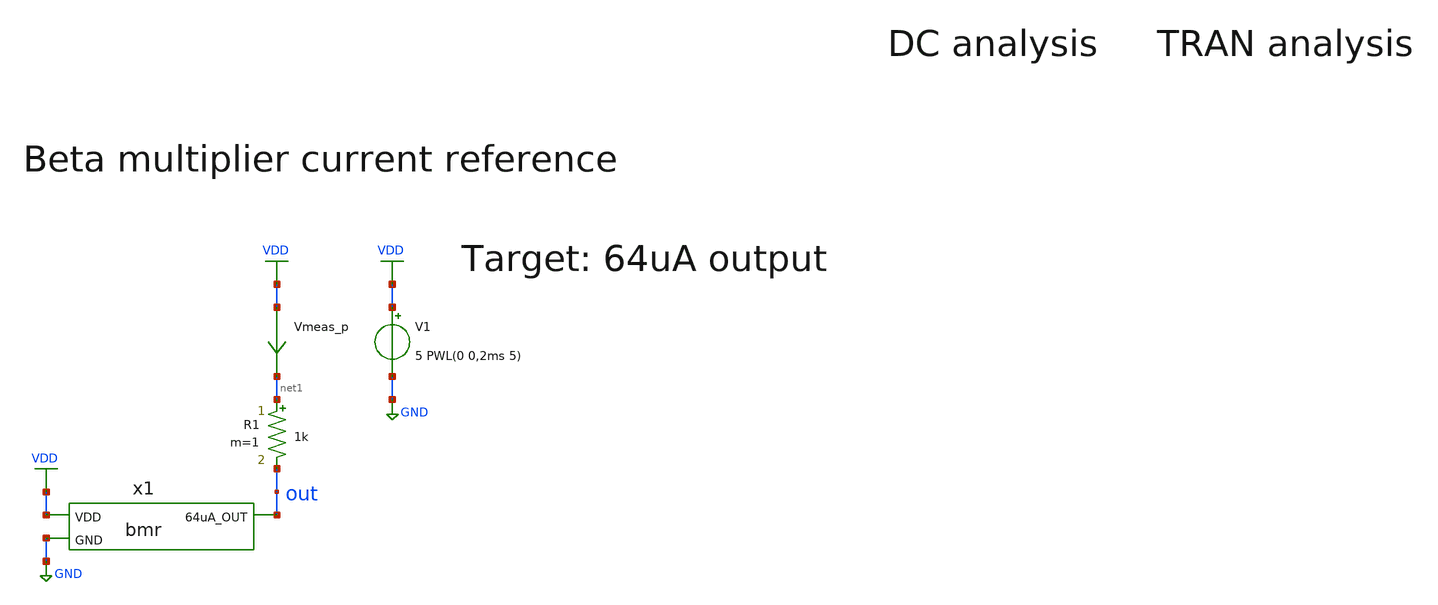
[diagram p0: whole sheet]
** sch_path: member_project/AM_Radio/Yamada3/xschem/tb_bmr.sch
* Copyright 2022 GlobalFoundries PDK Authors
* Licensed under the Apache License, Version 2.0 (the "License");
* you may not use this file except in compliance with the License.
* You may obtain a copy of the License at
* https://www.apache.org/licenses/LICENSE-2.0
* Unless required by applicable law or agreed to in writing, software
* distributed under the License is distributed on an "AS IS" BASIS,
* WITHOUT WARRANTIES OR CONDITIONS OF ANY KIND, either express or implied.
* See the License for the specific language governing permissions and
* limitations under the License.
**.subckt tb_bmr
V1 VDD GND 5 PWL(0 0,2ms 5)
Vmeas_p VDD net1 0
.save i(vmeas_p)
x1 VDD GND out bmr
R1 net1 out 1k m=1
**** begin user architecture code


.control
save all
save currents
* DC analysis
dc v1 0 5.5 0.1 r1 1k 50k 5k
write tb_bmr_dc.raw
meas dc current_p find i(vmeas_p) at=5

* TRANS analysis
tran 1u 5m
write tb_bmr_tran.raw
.endc


 .include $::LIB/ip62_models
**** end user architecture code
**.ends

* expanding   symbol:  bmr.sym # of pins=3
** sym_path: bmr.sym
** sch_path: bmr.sch
.subckt bmr VDD GND 64uA_OUT
*.ipin VDD
*.ipin GND
*.opin 64uA_OUT
XXM1 net3 net3 VDD VDD PMOS w=4u l=4u as=0 ad=0 ps=0 pd=0 nrd=0 nrs=0 m=1
XXM2 net3 net6 GND GND NMOS w=10u l=2u as=0 ad=0 ps=0 pd=0 nrd=0 nrs=0 m=1
XXM3 net4 net3 net6 GND NMOS w=10u l=1u as=0 ad=0 ps=0 pd=0 nrd=0 nrs=0 m=1
XXM4 net6 net4 net1 net1 PMOS w=30u l=2u as=0 ad=0 ps=0 pd=0 nrd=0 nrs=0 m=1
XXM5 net4 net4 net2 net2 PMOS w=30u l=2u as=0 ad=0 ps=0 pd=0 nrd=0 nrs=0 m=1
XXM7 net6 net6 GND GND NMOS w=10u l=2u as=0 ad=0 ps=0 pd=0 nrd=0 nrs=0 m=1
XXM8 net4 net6 net5 net5 NMOS w=40u l=2u as=0 ad=0 ps=0 pd=0 nrd=0 nrs=0 m=1
XR1 net5 GND VDD F_RR w=4e-06 R=1 l=27e-06 tc1=0 tc2=0
XXM6 net8 net4 net7 net7 PMOS w=30u l=2u as=0 ad=0 ps=0 pd=0 nrd=0 nrs=0 m=1
XXM9 net8 net8 net9 GND NMOS w=10u l=2u as=0 ad=0 ps=0 pd=0 nrd=0 nrs=0 m=1
XXM10 net9 net9 GND GND NMOS w=10u l=2u as=0 ad=0 ps=0 pd=0 nrd=0 nrs=0 m=1
XXM11 64uA_OUT net8 net10 GND NMOS w=10u l=2u as=0 ad=0 ps=0 pd=0 nrd=0 nrs=0 m=1
XXM12 net10 net9 GND GND NMOS w=10u l=2u as=0 ad=0 ps=0 pd=0 nrd=0 nrs=0 m=1
XXM13 net1 net2 VDD VDD PMOS w=30u l=2u as=0 ad=0 ps=0 pd=0 nrd=0 nrs=0 m=1
XXM14 net2 net2 VDD VDD PMOS w=30u l=2u as=0 ad=0 ps=0 pd=0 nrd=0 nrs=0 m=1
XXM15 net7 net2 VDD VDD PMOS w=30u l=2u as=0 ad=0 ps=0 pd=0 nrd=0 nrs=0 m=1
.ends

.GLOBAL VDD
.GLOBAL GND
.end
